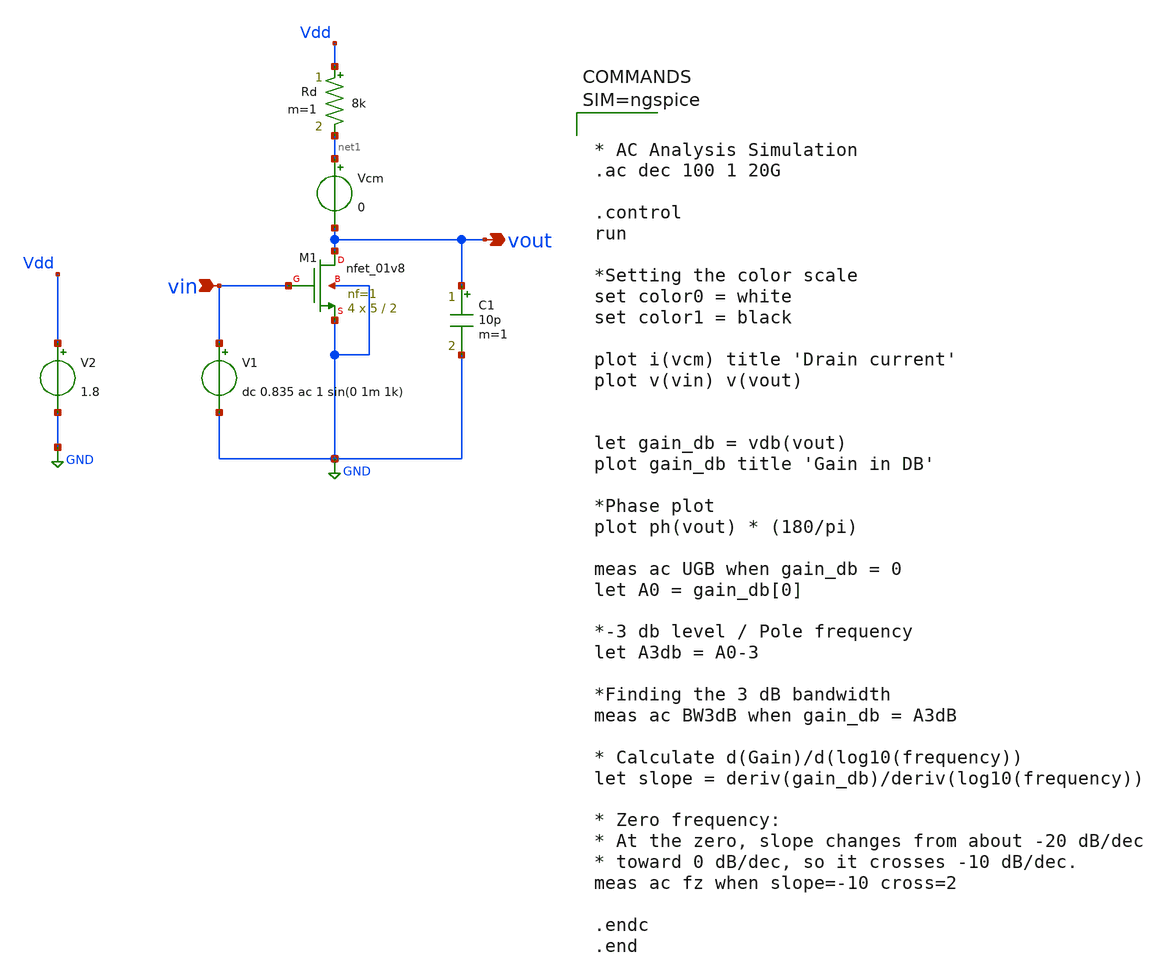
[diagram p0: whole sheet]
** sch_path: Common_Source_Restitive_Load_ckts/NMOS_CS_Amp_Res_load_AC_analysis.sch
**.subckt NMOS_CS_Amp_Res_load_AC_analysis vout vin
*.opin vout
*.ipin vin
XM1 vout vin GND GND sky130_fd_pr__nfet_01v8 L=2 W=5 nf=1 ad='int((1 + 1)/2) * 5 / 1 * 0.29' as='int((1 + 2)/2) * 5 / 1 * 0.29'
+ pd='2*int((1 + 1)/2) * (5 / 1 + 0.29)' ps='2*int((1 + 2)/2) * (5 / 1 + 0.29)' nrd='0.29 / 5 ' nrs='0.29 / 5 '
+ sa=0 sb=0 sd=0 mult=4 m=4
Rd Vdd net1 8k m=1
V1 vin GND dc 0.835 ac 1 sin(0 1m 1k)
V2 Vdd GND 1.8
Vcm net1 vout 0
C1 vout GND 10p m=1
**** begin user architecture code

** opencircuitdesign pdks install
.lib $::SKYWATER_MODELS/sky130.lib.spice tt




* AC Analysis Simulation
.ac dec 100 1 20G

.control
run

*Setting the color scale
set color0 = white
set color1 = black

plot i(vcm) title 'Drain current'
plot v(vin) v(vout)


let gain_db = vdb(vout)
plot gain_db title 'Gain in DB'

*Phase plot
plot ph(vout) * (180/pi)

meas ac UGB when gain_db = 0
let A0 = gain_db[0]

*-3 db level / Pole frequency
let A3db = A0-3

*Finding the 3 dB bandwidth
meas ac BW3dB when gain_db = A3dB

* Calculate d(Gain)/d(log10(frequency))
let slope = deriv(gain_db)/deriv(log10(frequency))

* Zero frequency:
* At the zero, slope changes from about -20 dB/dec
* toward 0 dB/dec, so it crosses -10 dB/dec.
meas ac fz when slope=-10 cross=2

.endc
.end




**** end user architecture code
**.ends
.GLOBAL GND
.end
